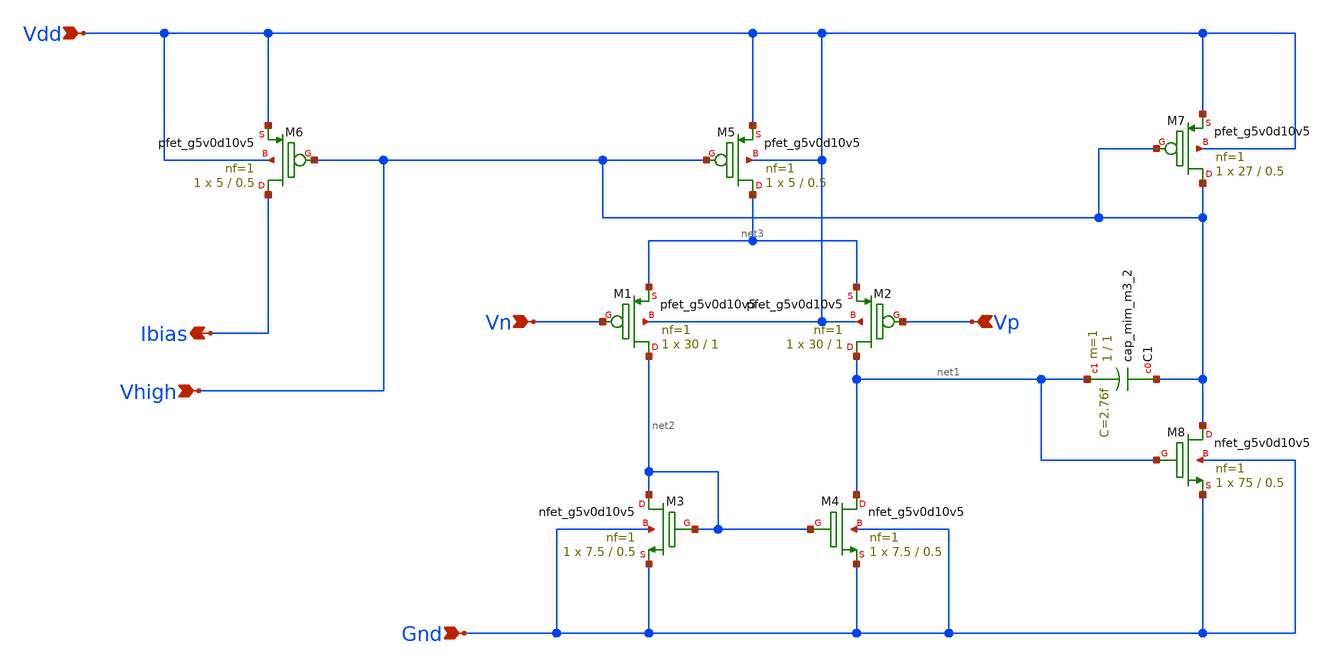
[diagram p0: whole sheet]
** sch_path: Bandgap/Schematics/BGR1.8v/Miller_OTA_PMOS_1.8.sch
**.subckt Miller_OTA_PMOS_1.8 Vp Vn Ibias Vdd Gnd Vhigh
*.ipin Vp
*.ipin Vn
*.opin Ibias
*.ipin Vdd
*.ipin Gnd
*.ipin Vhigh
XM6 Ibias Vhigh Vdd Vdd sky130_fd_pr__pfet_g5v0d10v5 L=0.5 W=5 nf=1 ad='int((nf+1)/2) * W/nf * 0.29'
+ as='int((nf+2)/2) * W/nf * 0.29' pd='2*int((nf+1)/2) * (W/nf + 0.29)' ps='2*int((nf+2)/2) * (W/nf + 0.29)'
+ nrd='0.29 / W' nrs='0.29 / W' sa=0 sb=0 sd=0 mult=1 m=1
XM5 net3 Vhigh Vdd Vdd sky130_fd_pr__pfet_g5v0d10v5 L=0.5 W=5 nf=1 ad='int((nf+1)/2) * W/nf * 0.29' as='int((nf+2)/2) * W/nf * 0.29'
+ pd='2*int((nf+1)/2) * (W/nf + 0.29)' ps='2*int((nf+2)/2) * (W/nf + 0.29)' nrd='0.29 / W' nrs='0.29 / W'
+ sa=0 sb=0 sd=0 mult=1 m=1
XM7 Vhigh Vhigh Vdd Vdd sky130_fd_pr__pfet_g5v0d10v5 L=0.5 W=27 nf=1 ad='int((nf+1)/2) * W/nf * 0.29'
+ as='int((nf+2)/2) * W/nf * 0.29' pd='2*int((nf+1)/2) * (W/nf + 0.29)' ps='2*int((nf+2)/2) * (W/nf + 0.29)'
+ nrd='0.29 / W' nrs='0.29 / W' sa=0 sb=0 sd=0 mult=1 m=1
XC1 Vhigh net1 sky130_fd_pr__cap_mim_m3_2 W=1 L=1 MF=1 m=1
XM2 net1 Vp net3 Vdd sky130_fd_pr__pfet_g5v0d10v5 L=1 W=30 nf=1 ad='int((nf+1)/2) * W/nf * 0.29' as='int((nf+2)/2) * W/nf * 0.29'
+ pd='2*int((nf+1)/2) * (W/nf + 0.29)' ps='2*int((nf+2)/2) * (W/nf + 0.29)' nrd='0.29 / W' nrs='0.29 / W'
+ sa=0 sb=0 sd=0 mult=1 m=1
XM1 net2 Vn net3 Vdd sky130_fd_pr__pfet_g5v0d10v5 L=1 W=30 nf=1 ad='int((nf+1)/2) * W/nf * 0.29' as='int((nf+2)/2) * W/nf * 0.29'
+ pd='2*int((nf+1)/2) * (W/nf + 0.29)' ps='2*int((nf+2)/2) * (W/nf + 0.29)' nrd='0.29 / W' nrs='0.29 / W'
+ sa=0 sb=0 sd=0 mult=1 m=1
XM8 Vhigh net1 Gnd Gnd sky130_fd_pr__nfet_g5v0d10v5 L=0.5 W=75 nf=1 ad='int((nf+1)/2) * W/nf * 0.29'
+ as='int((nf+2)/2) * W/nf * 0.29' pd='2*int((nf+1)/2) * (W/nf + 0.29)' ps='2*int((nf+2)/2) * (W/nf + 0.29)'
+ nrd='0.29 / W' nrs='0.29 / W' sa=0 sb=0 sd=0 mult=1 m=1
XM4 net1 net2 Gnd Gnd sky130_fd_pr__nfet_g5v0d10v5 L=0.5 W=7.5 nf=1 ad='int((nf+1)/2) * W/nf * 0.29'
+ as='int((nf+2)/2) * W/nf * 0.29' pd='2*int((nf+1)/2) * (W/nf + 0.29)' ps='2*int((nf+2)/2) * (W/nf + 0.29)'
+ nrd='0.29 / W' nrs='0.29 / W' sa=0 sb=0 sd=0 mult=1 m=1
XM3 net2 net2 Gnd Gnd sky130_fd_pr__nfet_g5v0d10v5 L=0.5 W=7.5 nf=1 ad='int((nf+1)/2) * W/nf * 0.29'
+ as='int((nf+2)/2) * W/nf * 0.29' pd='2*int((nf+1)/2) * (W/nf + 0.29)' ps='2*int((nf+2)/2) * (W/nf + 0.29)'
+ nrd='0.29 / W' nrs='0.29 / W' sa=0 sb=0 sd=0 mult=1 m=1
**.ends
.end
